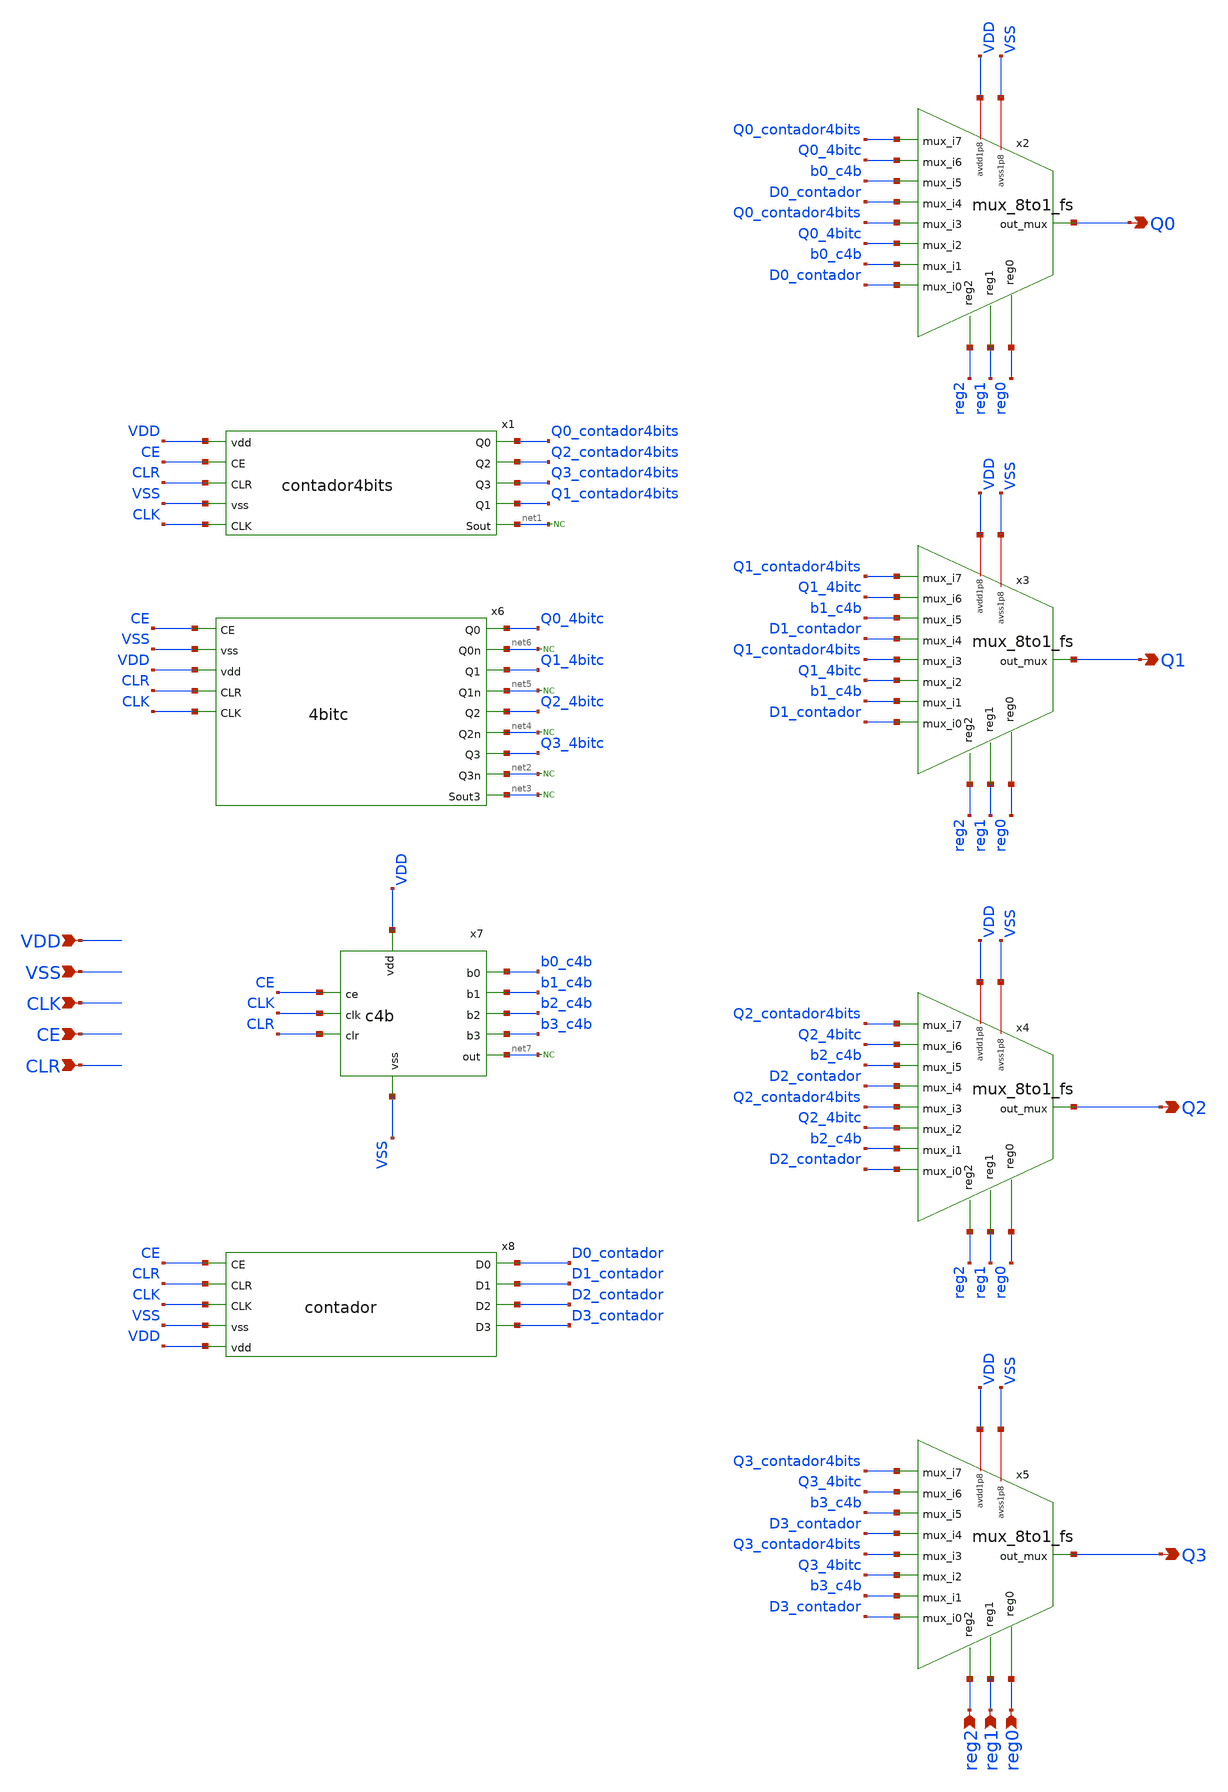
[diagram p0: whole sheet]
** sch_path: track_vlsi/toplevel_vlsi/sch/toplevel.sch
**.subckt toplevel VDD VSS CLK CE CLR reg2 reg1 reg0 Q0 Q1 Q2 Q3
*.ipin VDD
*.ipin VSS
*.ipin CLK
*.ipin CE
*.ipin CLR
*.ipin reg2
*.ipin reg1
*.ipin reg0
*.opin Q0
*.opin Q1
*.opin Q2
*.opin Q3
x2 VDD VSS Q0_contador4bits Q0_4bitc b0_c4b Q0 D0_contador Q0_contador4bits reg0 Q0_4bitc b0_c4b
+ D0_contador reg1 reg2 mux_8to1_fs
x3 VDD VSS Q1_contador4bits Q1_4bitc b1_c4b Q1 D1_contador Q1_contador4bits reg0 Q1_4bitc b1_c4b
+ D1_contador reg1 reg2 mux_8to1_fs
x4 VDD VSS Q2_contador4bits Q2_4bitc b2_c4b Q2 D2_contador Q2_contador4bits reg0 Q2_4bitc b2_c4b
+ D2_contador reg1 reg2 mux_8to1_fs
x5 VDD VSS Q3_contador4bits Q3_4bitc b3_c4b Q3 D3_contador Q3_contador4bits reg0 Q3_4bitc b3_c4b
+ D3_contador reg1 reg2 mux_8to1_fs
x6 Q0_4bitc CE net6 Q1_4bitc net5 Q2_4bitc net4 Q3_4bitc net2 net3 VSS VDD CLR CLK 4bitc
x7 CE CLK CLR VDD VSS b0_c4b b1_c4b b2_c4b b3_c4b net7 c4b
x8 D0_contador CE CLR CLK VSS VDD D1_contador D2_contador D3_contador contador
* noconn #net1
* noconn #net2
* noconn #net3
* noconn #net4
* noconn #net5
* noconn #net6
* noconn #net7
x1 VDD Q0_contador4bits Q2_contador4bits Q3_contador4bits Q1_contador4bits CE CLR net1 VSS CLK
+ contador4bits
**.ends
.end
